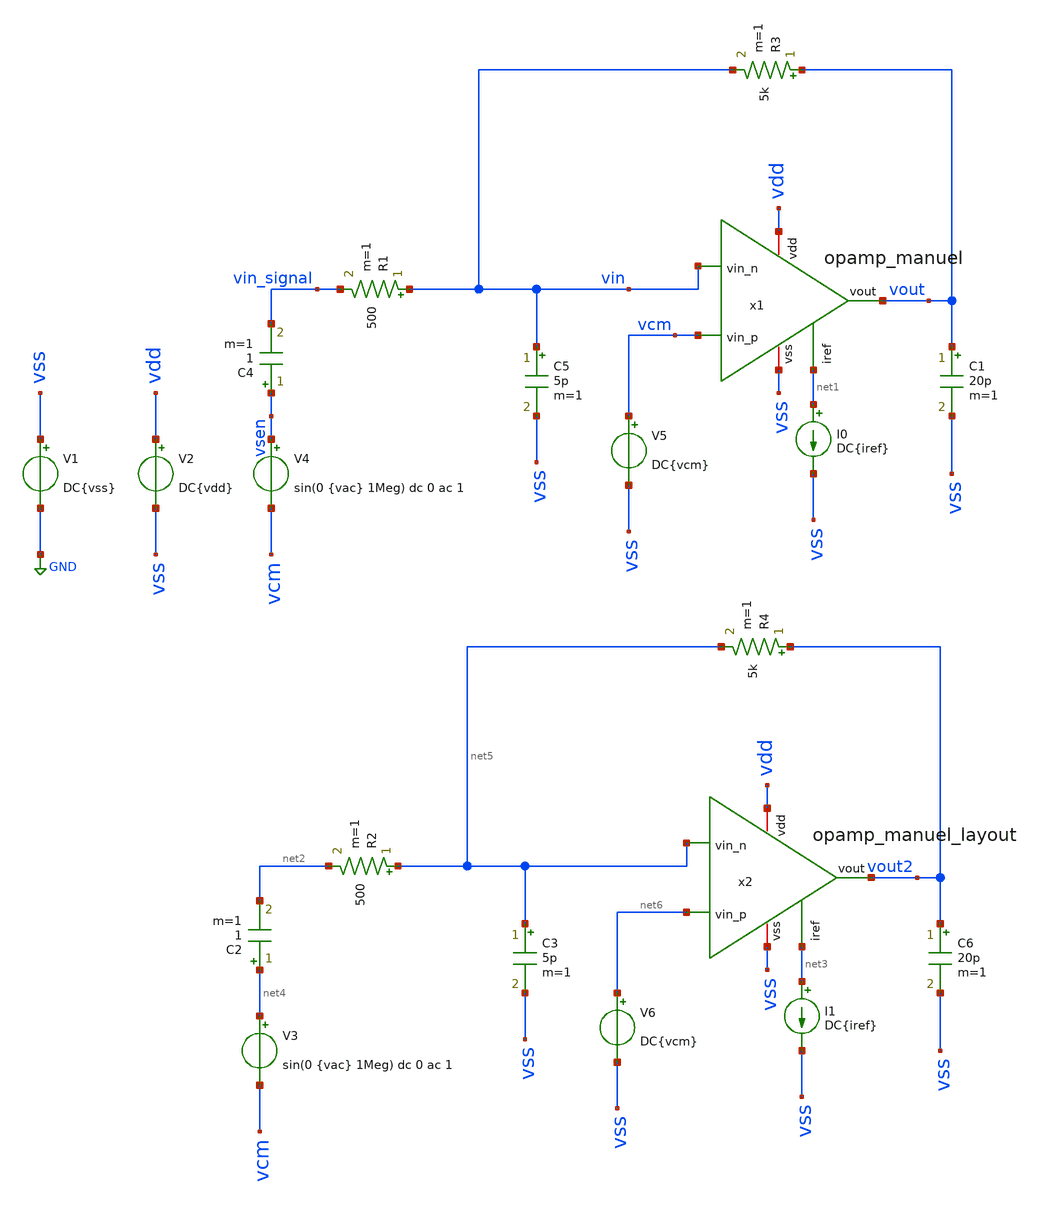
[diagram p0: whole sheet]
** sch_path: track_analogico/opamp_manuel/sch/opamp_closeloop.sch
**.subckt opamp_closeloop
V1 vss GND DC{vss}
V2 vdd vss DC{vdd}
V4 vsen vcm sin(0 {vac} 1Meg) dc 0 ac 1
C4 vsen vin_signal 1 m=1
I0 net1 vss DC{iref}
R1 vin vin_signal 500 m=1
R3 vout vin 5k m=1
C5 vin vss 5p m=1
C1 vout vss 20p m=1
V5 vcm vss DC{vcm}
x1 vdd net1 vin vcm vout vss opamp_manuel
V3 net4 vcm sin(0 {vac} 1Meg) dc 0 ac 1
C2 net4 net2 1 m=1
I1 net3 vss DC{iref}
R2 net5 net2 500 m=1
R4 vout2 net5 5k m=1
C3 net5 vss 5p m=1
C6 vout2 vss 20p m=1
V6 net6 vss DC{vcm}
x2 vdd net3 net5 net6 vout2 vss opamp_manuel_layout
**** begin user architecture code




* Circuit Parameters
.param vss = 0
.param vdd = 1.62
.param vac = 60m
.param vcm = vdd/2
.param iref = 95u

.options TEMP = 125

* Include Models
.lib ~/skywater/skywater-pdk/libraries/sky130_fd_pr_ngspice/latest/models/corners/sky130.lib SS
.include ~/caravel_eamta_2021/track_analogico/opamp_manuel/sch/simulations/opamp_manuel_layout.spice

* OP Parameters & Signals to save
.save all  @M.X1.XM1.msky130_fd_pr__pfet_01v8_lvt[id] @M.X1.XM1.msky130_fd_pr__pfet_01v8_lvt[vth] @M.X1.XM1.msky130_fd_pr__pfet_01v8_lvt[vgs] @M.X1.XM1.msky130_fd_pr__pfet_01v8_lvt[vds] @M.X1.XM1.msky130_fd_pr__pfet_01v8_lvt[vdsat] @M.X1.XM1.msky130_fd_pr__pfet_01v8_lvt[gm] @M.X1.XM1.msky130_fd_pr__pfet_01v8_lvt[gds]  @M.X1.XM2.msky130_fd_pr__pfet_01v8_lvt[id] @M.X1.XM2.msky130_fd_pr__pfet_01v8_lvt[vth] @M.X1.XM2.msky130_fd_pr__pfet_01v8_lvt[vgs] @M.X1.XM2.msky130_fd_pr__pfet_01v8_lvt[vds] @M.X1.XM2.msky130_fd_pr__pfet_01v8_lvt[vdsat] @M.X1.XM2.msky130_fd_pr__pfet_01v8_lvt[gm] @M.X1.XM2.msky130_fd_pr__pfet_01v8_lvt[gds]  @M.X1.XM3.msky130_fd_pr__nfet_01v8[id] @M.X1.XM3.msky130_fd_pr__nfet_01v8[vth] @M.X1.XM3.msky130_fd_pr__nfet_01v8[vgs] @M.X1.XM3.msky130_fd_pr__nfet_01v8[vds] @M.X1.XM3.msky130_fd_pr__nfet_01v8[vdsat] @M.X1.XM3.msky130_fd_pr__nfet_01v8[gm] @M.X1.XM3.msky130_fd_pr__nfet_01v8[gds]  @M.X1.XM4.msky130_fd_pr__nfet_01v8[id] @M.X1.XM4.msky130_fd_pr__nfet_01v8[vth] @M.X1.XM4.msky130_fd_pr__nfet_01v8[vgs] @M.X1.XM4.msky130_fd_pr__nfet_01v8[vds] @M.X1.XM4.msky130_fd_pr__nfet_01v8[vdsat] @M.X1.XM4.msky130_fd_pr__nfet_01v8[gm] @M.X1.XM4.msky130_fd_pr__nfet_01v8[gds]  @M.X1.XM5.msky130_fd_pr__pfet_01v8[id] @M.X1.XM5.msky130_fd_pr__pfet_01v8[vth] @M.X1.XM5.msky130_fd_pr__pfet_01v8[vgs] @M.X1.XM5.msky130_fd_pr__pfet_01v8[vds] @M.X1.XM5.msky130_fd_pr__pfet_01v8[vdsat] @M.X1.XM5.msky130_fd_pr__pfet_01v8[gm] @M.X1.XM5.msky130_fd_pr__pfet_01v8[gds]  @M.X1.XM6.msky130_fd_pr__nfet_01v8[id] @M.X1.XM6.msky130_fd_pr__nfet_01v8[vth] @M.X1.XM6.msky130_fd_pr__nfet_01v8[vgs] @M.X1.XM6.msky130_fd_pr__nfet_01v8[vds] @M.X1.XM6.msky130_fd_pr__nfet_01v8[vdsat] @M.X1.XM6.msky130_fd_pr__nfet_01v8[gm] @M.X1.XM6.msky130_fd_pr__nfet_01v8[gds]  @M.X1.XM7.msky130_fd_pr__pfet_01v8[id] @M.X1.XM7.msky130_fd_pr__pfet_01v8[vth] @M.X1.XM7.msky130_fd_pr__pfet_01v8[vgs] @M.X1.XM7.msky130_fd_pr__pfet_01v8[vds] @M.X1.XM7.msky130_fd_pr__pfet_01v8[vdsat] @M.X1.XM7.msky130_fd_pr__pfet_01v8[gm] @M.X1.XM7.msky130_fd_pr__pfet_01v8[gds]  @M.X1.XM8.msky130_fd_pr__pfet_01v8[id] @M.X1.XM8.msky130_fd_pr__pfet_01v8[vth] @M.X1.XM8.msky130_fd_pr__pfet_01v8[vgs] @M.X1.XM8.msky130_fd_pr__pfet_01v8[vds] @M.X1.XM8.msky130_fd_pr__pfet_01v8[vdsat] @M.X1.XM8.msky130_fd_pr__pfet_01v8[gm] @M.X1.XM8.msky130_fd_pr__pfet_01v8[gds]  @M.X1.XM6.msky130_fd_pr__nfet_01v8[cgs]  @M.X1.XM9.msky130_fd_pr__nfet_01v8[gds]

*Simulation
.control

* analisis AC
	ac dec 100 1k 500G

	write opamp_closeloop.raw

 	meas ac GBW when vdb(vout)=0
	meas ac DCG find vdb(vout) at=2k
 	meas ac GBW2 when vdb(vout2)=0
	meas ac DCG2 find vdb(vout2) at=2k

	print DCG
	print GBW
	print DCG2
	print GBW2

	plot vdb(vout) vp(vout)*180/PI title 'Transferencia a lazo cerrado'
	plot vdb(vout2) vp(vout2)*180/PI title 'Transferencia a lazo cerrado (parasitos)'

* analisis de punto de operacion
	reset
	op
	save all

	print V(vout)
	write opamp_closeloop.raw
.endc

.end


**** end user architecture code
**.ends
.GLOBAL GND
.end
